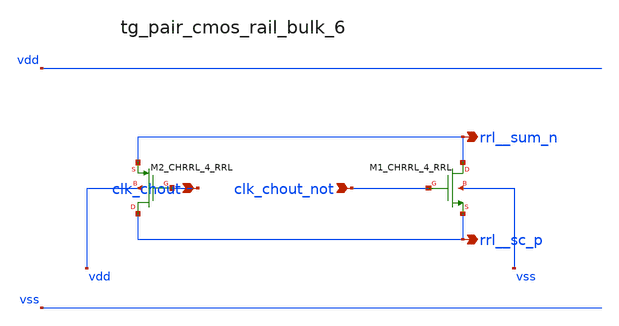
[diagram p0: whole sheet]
** sch_path: analog-db/raw/ia_004_fan_chopper_rrl/hier/blocks/tg_pair_cmos_rail_bulk_6.sch
**.subckt tg_pair_cmos_rail_bulk_6 clk_chout clk_chout_not rrl__sum_n rrl__sc_p
*.ipin clk_chout
*.ipin clk_chout_not
*.opin rrl__sum_n
*.opin rrl__sc_p
XM1_CHRRL_4_RRL rrl__sum_n clk_chout_not rrl__sc_p vss sg13_lv_nmos w=x_dut_xm1_chrrl_4_rrl_w
+ l=x_dut_xm1_chrrl_4_rrl_l ng=1 m=x_dut_xm1_chrrl_4_rrl_m
XM2_CHRRL_4_RRL rrl__sc_p clk_chout rrl__sum_n vdd sg13_lv_pmos w=x_dut_xm2_chrrl_4_rrl_w
+ l=x_dut_xm2_chrrl_4_rrl_l ng=1 m=x_dut_xm2_chrrl_4_rrl_m
**.ends
.end
